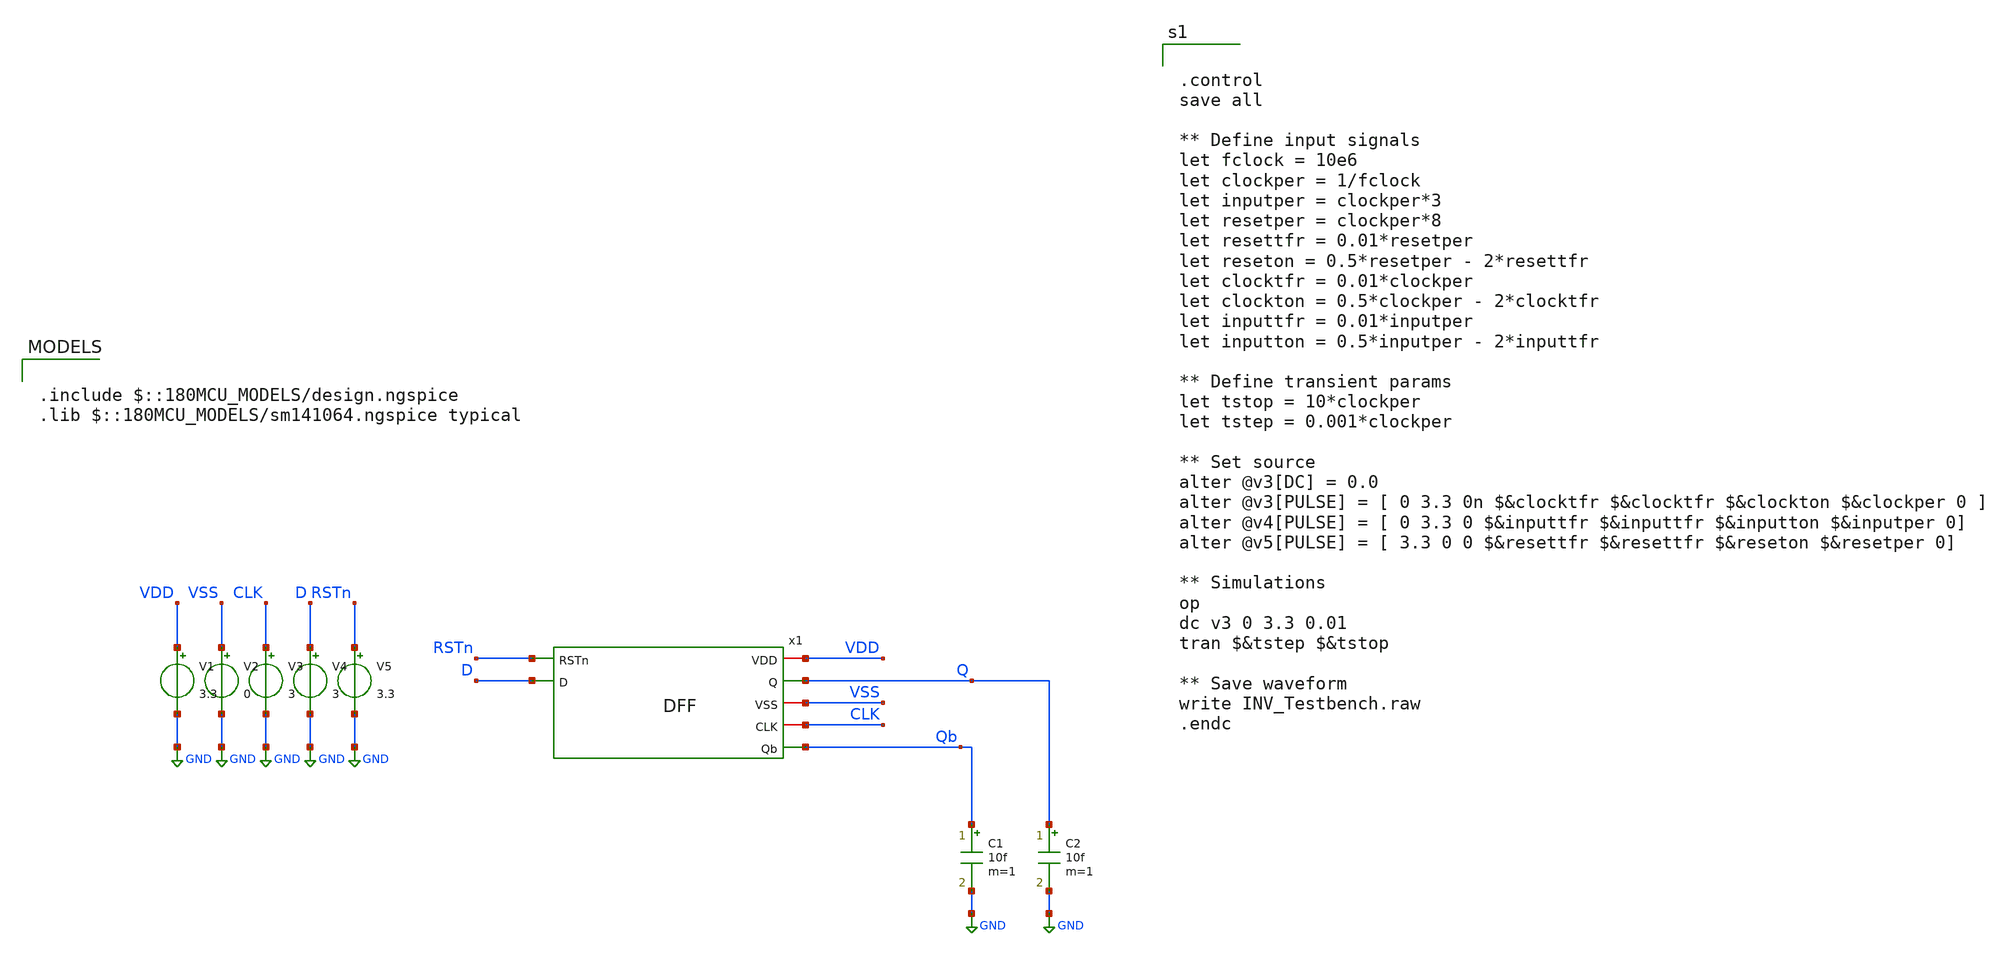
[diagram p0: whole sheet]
** sch_path: CAD6/DFF_Ray/DFF_Testbench.sch
**.subckt DFF_Testbench
V1 VDD GND 3.3
V2 VSS GND 0
V3 CLK GND 3
V4 D GND 3
V5 RSTn GND 3.3
C1 Qb GND 10f m=1
C2 Q GND 10f m=1
x1 RSTn VDD Q D VSS CLK Qb DFF
**** begin user architecture code

.include $::180MCU_MODELS/design.ngspice
.lib $::180MCU_MODELS/sm141064.ngspice typical



.control
save all

** Define input signals
let fclock = 10e6
let clockper = 1/fclock
let inputper = clockper*3
let resetper = clockper*8
let resettfr = 0.01*resetper
let reseton = 0.5*resetper - 2*resettfr
let clocktfr = 0.01*clockper
let clockton = 0.5*clockper - 2*clocktfr
let inputtfr = 0.01*inputper
let inputton = 0.5*inputper - 2*inputtfr

** Define transient params
let tstop = 10*clockper
let tstep = 0.001*clockper

** Set source
alter @v3[DC] = 0.0
alter @v3[PULSE] = [ 0 3.3 0n $&clocktfr $&clocktfr $&clockton $&clockper 0 ]
alter @v4[PULSE] = [ 0 3.3 0 $&inputtfr $&inputtfr $&inputton $&inputper 0]
alter @v5[PULSE] = [ 3.3 0 0 $&resettfr $&resettfr $&reseton $&resetper 0]

** Simulations
op
dc v3 0 3.3 0.01
tran $&tstep $&tstop

** Save waveform
write INV_Testbench.raw
.endc


**** end user architecture code
**.ends

* expanding   symbol:  CAD2/DFF.sym # of pins=7
** sym_path: CAD6/DFF_Ray/DFF.sym
** sch_path: CAD6/DFF_Ray/DFF.sch
.subckt DFF RSTn VDD Q D VSS CLK Qb
*.ipin D
*.ipin RSTn
*.opin Q
*.opin Qb
*.iopin CLK
*.iopin VDD
*.iopin VSS
x1 VDD c net6 D cbar VSS TRI_STATE_INV
x2 c VDD VSS net1 net6 cbar TGATE
x3 VDD net6 net2 VSS INV
x4 VDD net2 net1 RSTn VSS NAND2
x5 c VDD VSS net2 net4 cbar TGATE
x6 VDD net4 net3 RSTn VSS NAND2
x7 VDD c net4 net3 cbar VSS TRI_STATE_INV
x8 VDD net3 Q VSS INV
x9 VDD net3 net5 VSS INV
x10 VDD net5 Qb VSS INV
x11 VDD CLK cbar VSS INV
x12 VDD cbar c VSS INV
.ends


* expanding   symbol:  CAD2/TRI_STATE_INV.sym # of pins=6
** sym_path: CAD6/DFF_Ray/TRI_STATE_INV.sym
** sch_path: CAD6/DFF_Ray/TRI_STATE_INV.sch
.subckt TRI_STATE_INV VDD CLK OUT IN CLKN VSS
*.iopin VSS
*.iopin VDD
*.iopin CLK
*.iopin CLKN
*.ipin IN
*.opin OUT
XM1 net1 CLK VDD VDD pfet_03v3 L=0.28u W=4u nf=1 ad='int((nf+1)/2) * W/nf * 0.18u' as='int((nf+2)/2) * W/nf * 0.18u'
+ pd='2*int((nf+1)/2) * (W/nf + 0.18u)' ps='2*int((nf+2)/2) * (W/nf + 0.18u)' nrd='0.18u / W' nrs='0.18u / W'
+ sa=0 sb=0 sd=0 m=1
XM2 OUT IN net1 VDD pfet_03v3 L=0.28u W=4u nf=1 ad='int((nf+1)/2) * W/nf * 0.18u' as='int((nf+2)/2) * W/nf * 0.18u'
+ pd='2*int((nf+1)/2) * (W/nf + 0.18u)' ps='2*int((nf+2)/2) * (W/nf + 0.18u)' nrd='0.18u / W' nrs='0.18u / W'
+ sa=0 sb=0 sd=0 m=1
XM3 OUT IN net2 VSS nfet_03v3 L=0.28u W=2u nf=1 ad='int((nf+1)/2) * W/nf * 0.18u' as='int((nf+2)/2) * W/nf * 0.18u'
+ pd='2*int((nf+1)/2) * (W/nf + 0.18u)' ps='2*int((nf+2)/2) * (W/nf + 0.18u)' nrd='0.18u / W' nrs='0.18u / W'
+ sa=0 sb=0 sd=0 m=1
XM4 net2 CLKN VSS VSS nfet_03v3 L=0.28u W=2u nf=1 ad='int((nf+1)/2) * W/nf * 0.18u' as='int((nf+2)/2) * W/nf * 0.18u'
+ pd='2*int((nf+1)/2) * (W/nf + 0.18u)' ps='2*int((nf+2)/2) * (W/nf + 0.18u)' nrd='0.18u / W' nrs='0.18u / W'
+ sa=0 sb=0 sd=0 m=1
.ends


* expanding   symbol:  CAD2/TGATE.sym # of pins=6
** sym_path: CAD6/DFF_Ray/TGATE.sym
** sch_path: CAD6/DFF_Ray/TGATE.sch
.subckt TGATE CLK VDD VSS IN OUT CLKN
*.ipin IN
*.opin OUT
*.iopin CLKN
*.iopin CLK
*.iopin VDD
*.iopin VSS
XM1 IN CLK OUT VSS nfet_03v3 L=0.28u W=1u nf=1 ad='int((nf+1)/2) * W/nf * 0.18u' as='int((nf+2)/2) * W/nf * 0.18u'
+ pd='2*int((nf+1)/2) * (W/nf + 0.18u)' ps='2*int((nf+2)/2) * (W/nf + 0.18u)' nrd='0.18u / W' nrs='0.18u / W'
+ sa=0 sb=0 sd=0 m=1
XM2 IN CLKN OUT VDD pfet_03v3 L=0.28u W=2u nf=1 ad='int((nf+1)/2) * W/nf * 0.18u' as='int((nf+2)/2) * W/nf * 0.18u'
+ pd='2*int((nf+1)/2) * (W/nf + 0.18u)' ps='2*int((nf+2)/2) * (W/nf + 0.18u)' nrd='0.18u / W' nrs='0.18u / W'
+ sa=0 sb=0 sd=0 m=1
.ends


* expanding   symbol:  CAD2/INV.sym # of pins=4
** sym_path: CAD6/DFF_Ray/INV.sym
** sch_path: CAD6/DFF_Ray/INV.sch
.subckt INV vdd IN OUT vss
*.ipin IN
*.opin OUT
*.iopin vss
*.iopin vdd
XM1 OUT IN vss vss nfet_03v3 L=0.28u W=1u nf=1 ad='int((nf+1)/2) * W/nf * 0.18u' as='int((nf+2)/2) * W/nf * 0.18u'
+ pd='2*int((nf+1)/2) * (W/nf + 0.18u)' ps='2*int((nf+2)/2) * (W/nf + 0.18u)' nrd='0.18u / W' nrs='0.18u / W'
+ sa=0 sb=0 sd=0 m=1
XM2 OUT IN vdd vdd pfet_03v3 L=0.28u W=2u nf=1 ad='int((nf+1)/2) * W/nf * 0.18u' as='int((nf+2)/2) * W/nf * 0.18u'
+ pd='2*int((nf+1)/2) * (W/nf + 0.18u)' ps='2*int((nf+2)/2) * (W/nf + 0.18u)' nrd='0.18u / W' nrs='0.18u / W'
+ sa=0 sb=0 sd=0 m=1
.ends


* expanding   symbol:  CAD2/NAND2.sym # of pins=5
** sym_path: CAD6/DFF_Ray/NAND2.sym
** sch_path: CAD6/DFF_Ray/NAND2.sch
.subckt NAND2 vdd INO OUT IN1 vss
*.ipin INO
*.ipin IN1
*.iopin vdd
*.iopin vss
*.opin OUT
XM1 OUT INO net1 vss nfet_03v3 L=0.28u W=2u nf=1 ad='int((nf+1)/2) * W/nf * 0.18u' as='int((nf+2)/2) * W/nf * 0.18u'
+ pd='2*int((nf+1)/2) * (W/nf + 0.18u)' ps='2*int((nf+2)/2) * (W/nf + 0.18u)' nrd='0.18u / W' nrs='0.18u / W'
+ sa=0 sb=0 sd=0 m=1
XM2 net1 IN1 vss vss nfet_03v3 L=0.28u W=2u nf=1 ad='int((nf+1)/2) * W/nf * 0.18u' as='int((nf+2)/2) * W/nf * 0.18u'
+ pd='2*int((nf+1)/2) * (W/nf + 0.18u)' ps='2*int((nf+2)/2) * (W/nf + 0.18u)' nrd='0.18u / W' nrs='0.18u / W'
+ sa=0 sb=0 sd=0 m=1
XM3 OUT INO vdd vdd pfet_03v3 L=0.28u W=2u nf=1 ad='int((nf+1)/2) * W/nf * 0.18u' as='int((nf+2)/2) * W/nf * 0.18u'
+ pd='2*int((nf+1)/2) * (W/nf + 0.18u)' ps='2*int((nf+2)/2) * (W/nf + 0.18u)' nrd='0.18u / W' nrs='0.18u / W'
+ sa=0 sb=0 sd=0 m=1
XM4 OUT IN1 vdd vdd pfet_03v3 L=0.28u W=2u nf=1 ad='int((nf+1)/2) * W/nf * 0.18u' as='int((nf+2)/2) * W/nf * 0.18u'
+ pd='2*int((nf+1)/2) * (W/nf + 0.18u)' ps='2*int((nf+2)/2) * (W/nf + 0.18u)' nrd='0.18u / W' nrs='0.18u / W'
+ sa=0 sb=0 sd=0 m=1
.ends

.GLOBAL GND
.end
